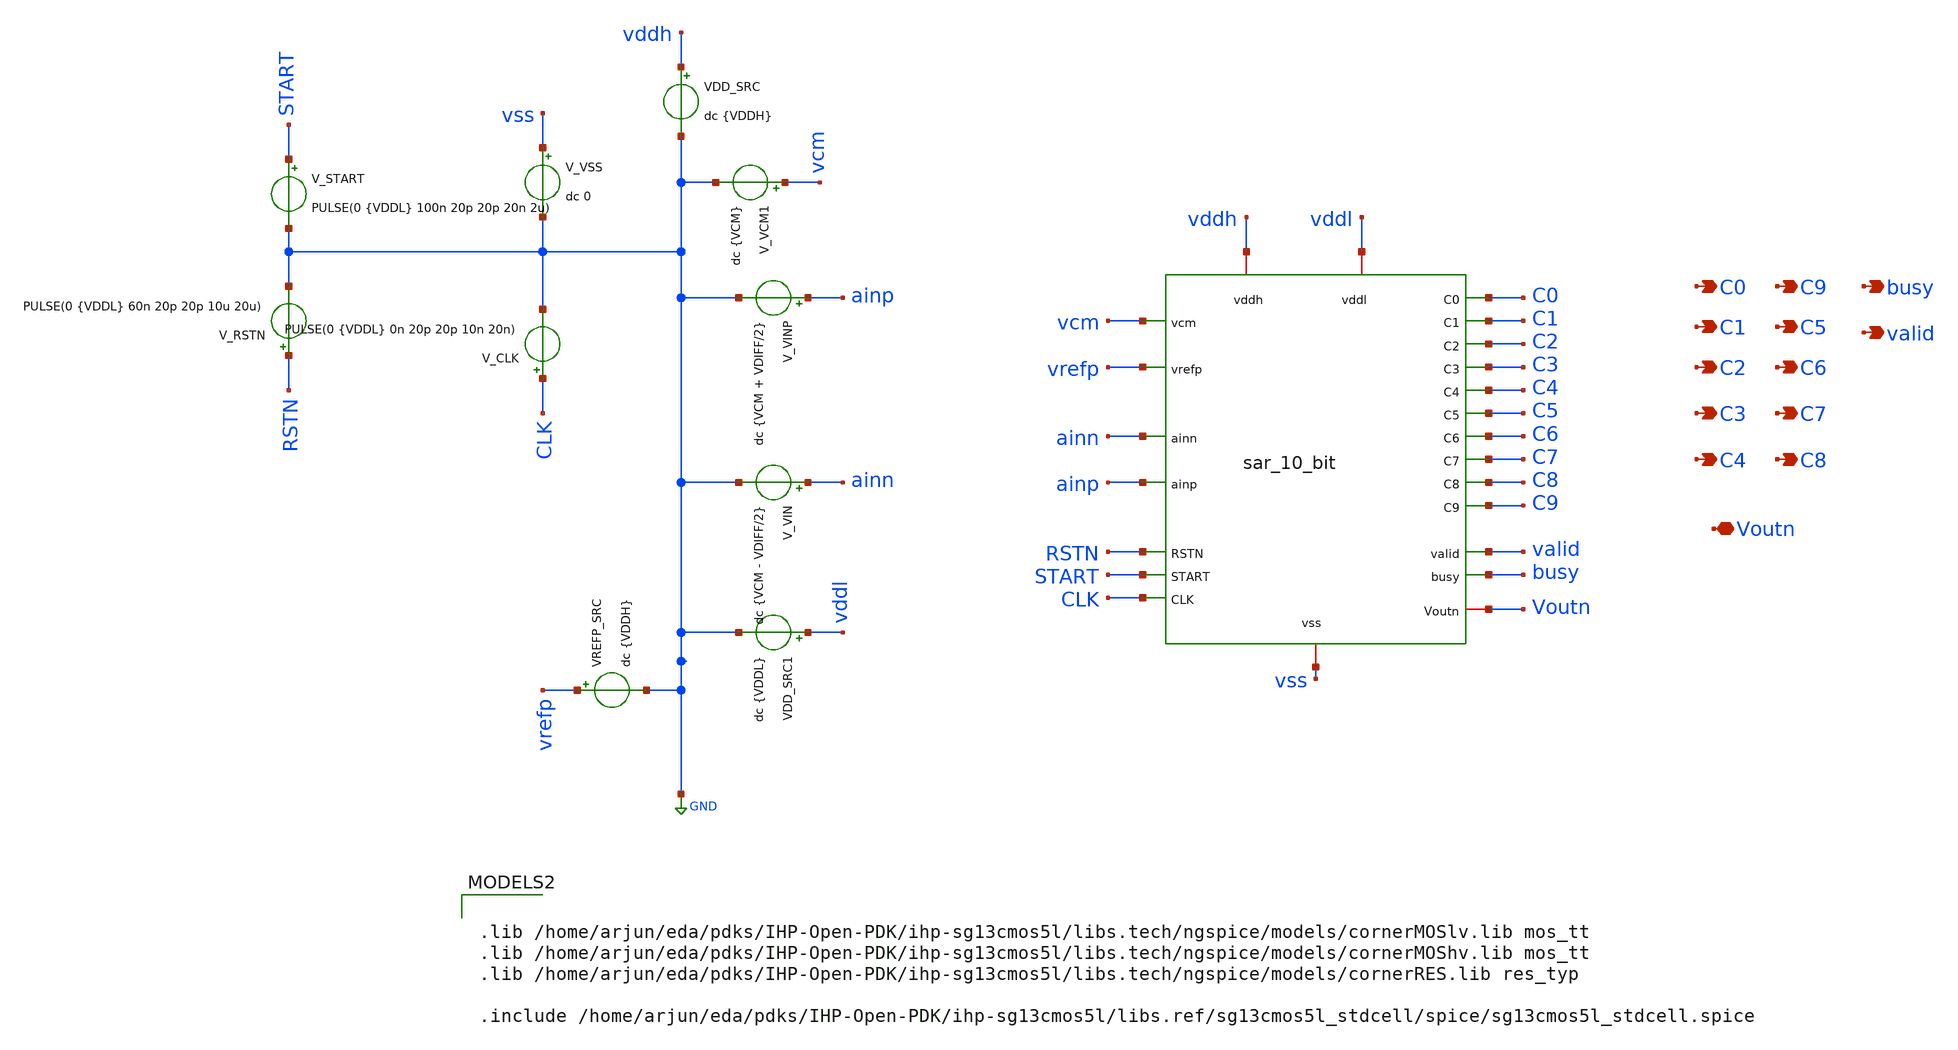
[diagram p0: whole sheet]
** sch_path: circuit_files/sar_adc_test/tb/sar_10_bit_tb.sch
**.subckt sar_10_bit_tb C1 C2 C3 C4 C5 C6 C7 C8 C0 C9 busy valid Voutn
*.opin C1
*.opin C2
*.opin C3
*.opin C4
*.opin C5
*.opin C6
*.opin C7
*.opin C8
*.opin C0
*.opin C9
*.opin busy
*.opin valid
*.iopin Voutn
x1 RSTN busy START valid vcm vrefp ainn ainp CLK C0 C9 C1 C5 C6 C2 C7 C3 C8 C4 vss vddh Voutn vddl
+ sar_10_bit
V_VIN ainn GND dc {VCM - VDIFF/2}
VDD_SRC vddh GND dc {VDDH}
V_VINP ainp GND dc {VCM + VDIFF/2}
V_VSS vss GND dc 0
V_CLK CLK GND PULSE(0 {VDDL} 0n 20p 20p 10n 20n)
V_VCM1 vcm GND dc {VCM}
VREFP_SRC vrefp GND dc {VDDH}
V_RSTN RSTN GND PULSE(0 {VDDL} 60n 20p 20p 10u 20u)
V_START START GND PULSE(0 {VDDL} 100n 20p 20p 20n 2u)
VDD_SRC1 vddl GND dc {VDDL}
**** begin user architecture code



.control

set noaskquit
set num_threads=6
reset

tran 20p 1.6u

let logic_th_lv = 0.6
let logic_th_hv = 1.65

meas tran ainp_dc FIND v(ainp) AT=90n
meas tran ainn_dc FIND v(ainn) AT=90n

let vin_diff = ainp_dc-ainn_dc


meas tran vddl_check FIND v(vddl) AT=90n
meas tran vddh_check FIND v(vddh) AT=90n

meas tran rstn_hi MAX v(RSTN) FROM=60n TO=90n

meas tran start_hi MAX v(START) FROM=100n TO=120n


meas tran busy_max MAX v(busy) FROM=100n TO=1.6u

meas tran valid_max MAX v(valid) FROM=100n TO=1.6u


let pass_busy=0
if busy_max > logic_th_lv
  let pass_busy=1
end


let pass_valid=0
if valid_max > logic_th_lv
  let pass_valid=1
end


let t_debug = 1.55u

if valid_max > logic_th_lv

  meas tran t_valid WHEN v(valid)=0.6 RISE=1

  let t_debug=t_valid+5n

end


meas tran sample_lv_max MAX v(x1.sample) FROM=100n TO=1.5u
meas tran sample_hv_max MAX v(x1.sample_hv) FROM=100n TO=1.5u

meas tran sample_lv_min MIN v(x1.sample) FROM=100n TO=1.5u
meas tran sample_hv_min MIN v(x1.sample_hv) FROM=100n TO=1.5u


let pass_sample_ls=0

if sample_lv_max > 1.08
  if sample_hv_max > 3.0
    if sample_lv_min < 0.12
      if sample_hv_min < 0.3
        let pass_sample_ls=1
      end
    end
  end
end


meas tran cclk_lv_max MAX v(x1.comp_clk) FROM=100n TO=1.5u
meas tran cclk_hv_max MAX v(x1.comp_clk_hv) FROM=100n TO=1.5u

meas tran cclk_lv_min MIN v(x1.comp_clk) FROM=100n TO=1.5u
meas tran cclk_hv_min MIN v(x1.comp_clk_hv) FROM=100n TO=1.5u


let pass_clk_ls=0

if cclk_lv_max > 1.08
  if cclk_hv_max > 3.0
    if cclk_lv_min < 0.12
      if cclk_hv_min < 0.3
        let pass_clk_ls=1
      end
    end
  end
end


meas tran comp_lv_max MAX v(x1.comp_lv) FROM=100n TO=1.5u
meas tran comp_lv_min MIN v(x1.comp_lv) FROM=100n TO=1.5u

meas tran voutp_max MAX v(x1.Voutp) FROM=100n TO=1.5u
meas tran voutp_min MIN v(x1.Voutp) FROM=100n TO=1.5u

meas tran voutn_max MAX v(Voutn) FROM=100n TO=1.5u
meas tran voutn_min MIN v(Voutn) FROM=100n TO=1.5u


let pass_comp_ls=0

if comp_lv_max > 1.08
  if comp_lv_min < 0.12
    let pass_comp_ls=1
  end
end


meas tran gatep_max MAX v(x1.x26.gatep) FROM=100n TO=1.5u
meas tran gatep_min MIN v(x1.x26.gatep) FROM=100n TO=1.5u

meas tran gaten_max MAX v(x1.x26.gaten) FROM=100n TO=1.5u
meas tran gaten_min MIN v(x1.x26.gaten) FROM=100n TO=1.5u


meas tran vcp_final FIND v(x1.vcp) AT=$&t_debug
meas tran vcn_final FIND v(x1.vcn) AT=$&t_debug

let vcdac_diff=vcp_final-vcn_final


meas tran c9v FIND v(C9) AT=$&t_debug
meas tran c8v FIND v(C8) AT=$&t_debug
meas tran c7v FIND v(C7) AT=$&t_debug
meas tran c6v FIND v(C6) AT=$&t_debug
meas tran c5v FIND v(C5) AT=$&t_debug
meas tran c4v FIND v(C4) AT=$&t_debug
meas tran c3v FIND v(C3) AT=$&t_debug
meas tran c2v FIND v(C2) AT=$&t_debug
meas tran c1v FIND v(C1) AT=$&t_debug
meas tran c0v FIND v(C0) AT=$&t_debug


let b9=0
if c9v > logic_th_lv
  let b9=1
end

let b8=0
if c8v > logic_th_lv
  let b8=1
end

let b7=0
if c7v > logic_th_lv
  let b7=1
end

let b6=0
if c6v > logic_th_lv
  let b6=1
end

let b5=0
if c5v > logic_th_lv
  let b5=1
end

let b4=0
if c4v > logic_th_lv
  let b4=1
end

let b3=0
if c3v > logic_th_lv
  let b3=1
end

let b2=0
if c2v > logic_th_lv
  let b2=1
end

let b1=0
if c1v > logic_th_lv
  let b1=1
end

let b0=0
if c0v > logic_th_lv
  let b0=1
end


let adc_code = 512*b9 + 256*b8 + 128*b7 + 64*b6 + 32*b5 + 16*b4 + 8*b3 + 4*b2 + 2*b1 + b0
echo ADC_CODE
print adc_code

meas tran dbp9_lv FIND v(x1.dbp9) AT=$&t_debug
meas tran dbp9_hv FIND v(x1.dbp9_hv) AT=$&t_debug

meas tran dbn9_lv FIND v(x1.dbn9) AT=$&t_debug
meas tran dbn9_hv FIND v(x1.dbn9_hv) AT=$&t_debug

meas tran bp9v FIND v(x1.bp9) AT=$&t_debug
meas tran bp8v FIND v(x1.bp8) AT=$&t_debug
meas tran bp7v FIND v(x1.bp7) AT=$&t_debug
meas tran bp6v FIND v(x1.bp6) AT=$&t_debug
meas tran bp5v FIND v(x1.bp5) AT=$&t_debug
meas tran bp4v FIND v(x1.bp4) AT=$&t_debug
meas tran bp3v FIND v(x1.bp3) AT=$&t_debug
meas tran bp2v FIND v(x1.bp2) AT=$&t_debug
meas tran bp1v FIND v(x1.bp1) AT=$&t_debug
meas tran bp0v FIND v(x1.bp0) AT=$&t_debug

meas tran bn9v FIND v(x1.bn9) AT=$&t_debug
meas tran bn8v FIND v(x1.bn8) AT=$&t_debug
meas tran bn7v FIND v(x1.bn7) AT=$&t_debug
meas tran bn6v FIND v(x1.bn6) AT=$&t_debug
meas tran bn5v FIND v(x1.bn5) AT=$&t_debug
meas tran bn4v FIND v(x1.bn4) AT=$&t_debug
meas tran bn3v FIND v(x1.bn3) AT=$&t_debug
meas tran bn2v FIND v(x1.bn2) AT=$&t_debug
meas tran bn1v FIND v(x1.bn1) AT=$&t_debug
meas tran bn0v FIND v(x1.bn0) AT=$&t_debug


meas tran h2l_q_max MAX v(x1.x26.q) FROM=100n TO=1.5u
meas tran h2l_q_min MIN v(x1.x26.q) FROM=100n TO=1.5u

meas tran h2l_qb_max MAX v(x1.x26.qb) FROM=100n TO=1.5u
meas tran h2l_qb_min MIN v(x1.x26.qb) FROM=100n TO=1.5u

meas tran h2l_hbuf2_max MAX v(x1.x26.hbuf2) FROM=100n TO=1.5u
meas tran h2l_hbuf2_min MIN v(x1.x26.hbuf2) FROM=100n TO=1.5u

meas tran h2l_out_max MAX v(x1.comp_lv) FROM=100n TO=1.5u
meas tran h2l_out_min MIN v(x1.comp_lv) FROM=100n TO=1.5u

meas tran iddh_avg AVG i(VDD_SRC) FROM=100n TO=1.5u
meas tran iddl_avg AVG i(VDD_SRC1) FROM=100n TO=1.5u

let pavg_hv=-3.3*iddh_avg
let pavg_lv=-1.2*iddl_avg

let pavg_total=pavg_hv+pavg_lv


let pass_total=0

if pass_busy > 0.5
  if pass_valid > 0.5
    if pass_sample_ls > 0.5
      if pass_clk_ls > 0.5
        if pass_comp_ls > 0.5
          let pass_total=1
        end
      end
    end
  end
end


echo .
echo IHP 10 BIT SAR ADC INTEGRATED NOMINAL TEST
echo .

echo SUPPLIES
print vddl_check
print vddh_check
echo .

echo INPUT
print ainp_dc
print ainn_dc
print vin_diff
echo .

echo FSM
print busy_max
print valid_max
print t_debug
echo .

echo SAMPLE_LEVEL_SHIFT
print sample_lv_min
print sample_lv_max
print sample_hv_min
print sample_hv_max
echo .

echo COMPARATOR_CLOCK_LEVEL_SHIFT
print cclk_lv_min
print cclk_lv_max
print cclk_hv_min
print cclk_hv_max
echo .

echo COMPARATOR
print voutp_min
print voutp_max
print voutn_min
print voutn_max
echo .

echo COMPARATOR_H2L
print comp_lv_min
print comp_lv_max
echo .

echo H2L_INTERNAL
print h2l_q_max
print h2l_q_min
print h2l_qb_max
print h2l_qb_min
print h2l_hbuf2_max
print h2l_hbuf2_min
print h2l_out_max
print h2l_out_min
echo .

echo CDAC_FINAL
print vcp_final
print vcn_final
print vcdac_diff
echo .

echo CODE_BITS
print b9
print b8
print b7
print b6
print b5
print b4
print b3
print b2
print b1
print b0
echo .

echo ADC_CODE
print adc_code
echo .

echo MSB_LEVEL_SHIFT
print dbp9_lv
print dbp9_hv
print dbn9_lv
print dbn9_hv
echo .

echo POWER_WATTS
print pavg_hv
print pavg_lv
print pavg_total
echo .

echo PASS_FLAGS
print pass_busy
print pass_valid
print pass_sample_ls
print pass_clk_ls
print pass_comp_ls
print pass_total

echo .
echo END


plot v(CLK) v(RSTN) v(START)

plot v(busy) v(valid)

plot v(x1.sample) v(x1.sample_hv) v(x1.sampleb_hv)

plot v(x1.comp_clk) v(x1.comp_clk_hv)

plot v(x1.Voutp) v(Voutn) v(x1.comp_lv)

plot v(x1.vcp) v(x1.vcn)

plot v(x1.dbp9) v(x1.dbp9_hv)

plot v(x1.dbn9) v(x1.dbn9_hv)

plot v(C9) v(C8) v(C7) v(C6) v(C5)

plot v(C4) v(C3) v(C2) v(C1) v(C0)

.endc




.lib /home/arjun/eda/pdks/IHP-Open-PDK/ihp-sg13cmos5l/libs.tech/ngspice/models/cornerMOSlv.lib mos_tt
.lib /home/arjun/eda/pdks/IHP-Open-PDK/ihp-sg13cmos5l/libs.tech/ngspice/models/cornerMOShv.lib mos_tt
.lib /home/arjun/eda/pdks/IHP-Open-PDK/ihp-sg13cmos5l/libs.tech/ngspice/models/cornerRES.lib res_typ

.include /home/arjun/eda/pdks/IHP-Open-PDK/ihp-sg13cmos5l/libs.ref/sg13cmos5l_stdcell/spice/sg13cmos5l_stdcell.spice





.param VDDH=3.3
.param VDDL=1.2

.param VREF=3.3
.param VCM=1.65

.param NBITS=10
.param Cu=10f

* LSB = 3.3 / 1024 = 3.22265625 mV
.param VDIFF=0.001611328125


.options savecurrents
.options reltol=1e-4
.options abstol=1e-12
.options vntol=1e-6

.options method=gear
.options maxord=2

.options plotwinsize=0
.options itl4=500

.save v(vddh)
.save v(vddl)
.save v(vss)

.save v(CLK)
.save v(RSTN)
.save v(START)

.save v(ainp)
.save v(ainn)

.save v(vrefp)
.save v(vcm)

.save v(busy)
.save v(valid)

.save v(C9)
.save v(C8)
.save v(C7)
.save v(C6)
.save v(C5)
.save v(C4)
.save v(C3)
.save v(C2)
.save v(C1)
.save v(C0)

.save v(Voutn)

.save v(x1.sample)
.save v(x1.comp_clk)
.save v(x1.comp_lv)

.save v(x1.dbp9)
.save v(x1.dbp8)
.save v(x1.dbp7)
.save v(x1.dbp6)
.save v(x1.dbp5)
.save v(x1.dbp4)
.save v(x1.dbp3)
.save v(x1.dbp2)
.save v(x1.dbp1)
.save v(x1.dbp0)

.save v(x1.dbn9)
.save v(x1.dbn8)
.save v(x1.dbn7)
.save v(x1.dbn6)
.save v(x1.dbn5)
.save v(x1.dbn4)
.save v(x1.dbn3)
.save v(x1.dbn2)
.save v(x1.dbn1)
.save v(x1.dbn0)

.save v(x1.sample_hv)
.save v(x1.sampleb_hv)

.save v(x1.comp_clk_hv)

.save v(x1.dbp9_hv)
.save v(x1.dbp8_hv)
.save v(x1.dbp7_hv)
.save v(x1.dbp6_hv)
.save v(x1.dbp5_hv)
.save v(x1.dbp4_hv)
.save v(x1.dbp3_hv)
.save v(x1.dbp2_hv)
.save v(x1.dbp1_hv)
.save v(x1.dbp0_hv)

.save v(x1.dbn9_hv)
.save v(x1.dbn8_hv)
.save v(x1.dbn7_hv)
.save v(x1.dbn6_hv)
.save v(x1.dbn5_hv)
.save v(x1.dbn4_hv)
.save v(x1.dbn3_hv)
.save v(x1.dbn2_hv)
.save v(x1.dbn1_hv)
.save v(x1.dbn0_hv)

.save v(x1.vcp)
.save v(x1.vcn)

.save v(x1.Voutp)

.save v(x1.bp9)
.save v(x1.bp8)
.save v(x1.bp7)
.save v(x1.bp6)
.save v(x1.bp5)
.save v(x1.bp4)
.save v(x1.bp3)
.save v(x1.bp2)
.save v(x1.bp1)
.save v(x1.bp0)

.save v(x1.bn9)
.save v(x1.bn8)
.save v(x1.bn7)
.save v(x1.bn6)
.save v(x1.bn5)
.save v(x1.bn4)
.save v(x1.bn3)
.save v(x1.bn2)
.save v(x1.bn1)
.save v(x1.bn0)


.save v(x1.x26.enb)

.save v(x1.x26.gatep)
.save v(x1.x26.gaten)

.save v(x1.x26.q)
.save v(x1.x26.qb)

.save v(x1.x26.hbuf)
.save v(x1.x26.hbuf2)
.save v(x1.x26.lvbuf)

.save i(VDD_SRC)
.save i(VDD_SRC1)




**** end user architecture code
**.ends
.GLOBAL GND
.end
